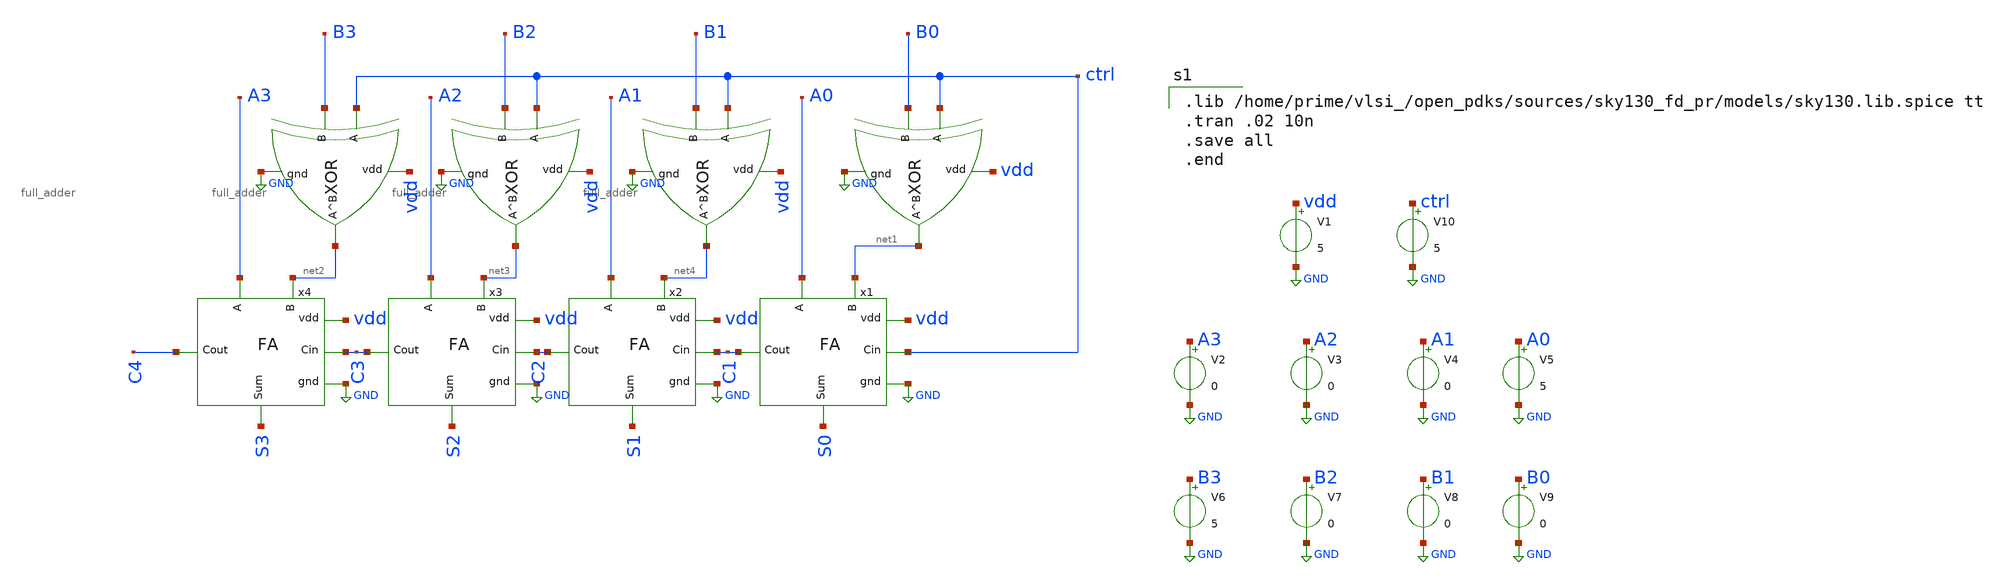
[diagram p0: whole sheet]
** sch_path: schematics/adder_subtractor.sch
**.subckt adder_subtractor
x1 S0 C1 ctrl vdd GND A0 net1 full_adder
x2 S1 C2 C1 vdd GND A1 net4 full_adder
x3 S2 C3 C2 vdd GND A2 net3 full_adder
x4 S3 C4 C3 vdd GND A3 net2 full_adder
x5 vdd GND net1 ctrl B0 xor
x6 vdd GND net4 ctrl B1 xor
x7 vdd GND net3 ctrl B2 xor
x8 vdd GND net2 ctrl B3 xor
V1 vdd GND 5
V2 A3 GND 0
V3 A2 GND 0
V4 A1 GND 0
V5 A0 GND 5
V6 B3 GND 5
V7 B2 GND 0
V8 B1 GND 0
V9 B0 GND 0
V10 ctrl GND 5
**** begin user architecture code

.lib /home/prime/vlsi_/open_pdks/sources/sky130_fd_pr/models/sky130.lib.spice tt
.tran .02 10n
.save all
.end

**** end user architecture code
**.ends
.GLOBAL GND
.end
